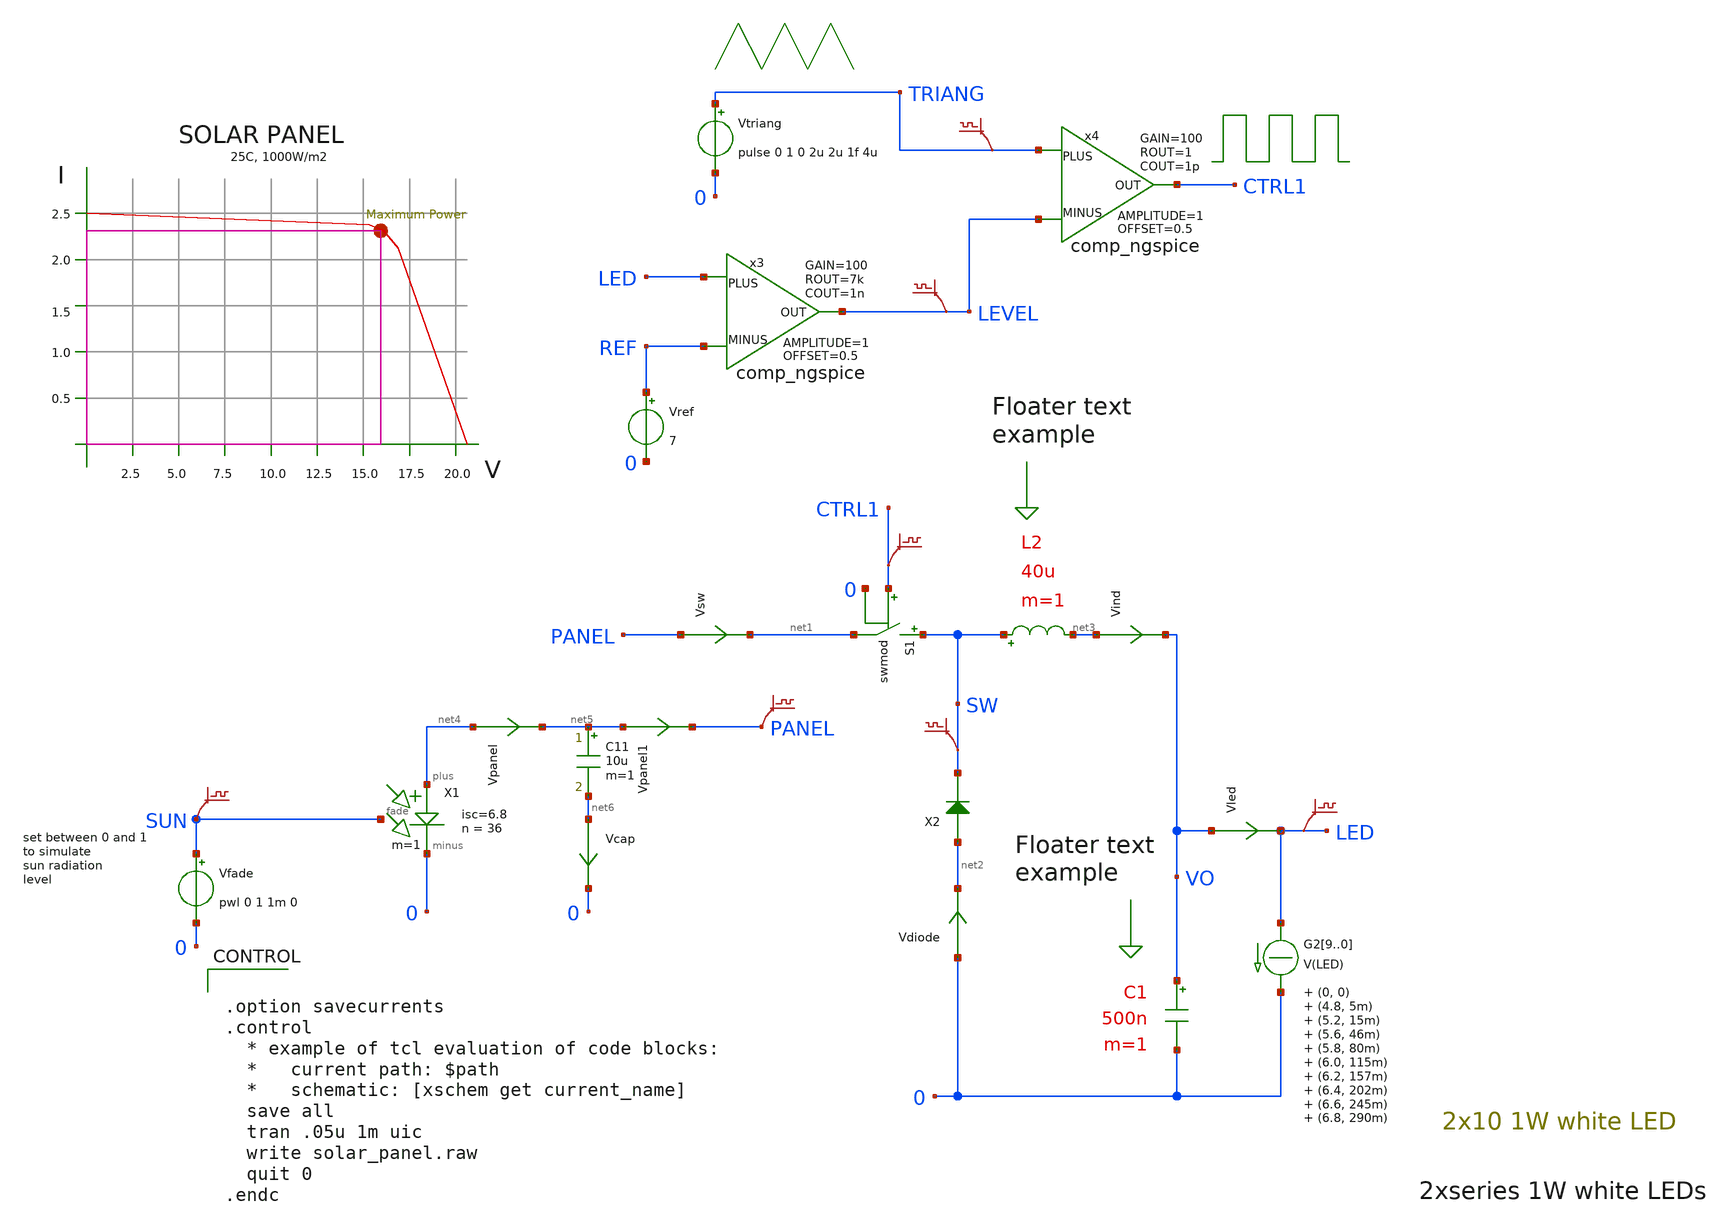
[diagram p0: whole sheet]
** sch_path: xschem_library/ngspice/solar_panel.sch
* Copyright (C) 1998-2024 Stefan Frederik Schippers
* This program is free software; you can redistribute it and/or modify
* it under the terms of the GNU General Public License as published by
* the Free Software Foundation; either version 2 of the License, or
* (at your option) any later version.
* This program is distributed in the hope that it will be useful,
* but WITHOUT ANY WARRANTY; without even the implied warranty of
* MERCHANTABILITY or FITNESS FOR A PARTICULAR PURPOSE.  See the
* GNU General Public License for more details.
* You should have received a copy of the GNU General Public License
* along with this program; if not, write to the Free Software
**.subckt solar_panel
Vled VO LED 0
.save i(vled)
L2 SW net3 40u m=1
C1 VO 0 500n m=1
Vind net3 VO 0
.save i(vind)
G29 LED 0 TABLE { V(LED) } = (0, 0) (4.8, 5m) (5.2, 15m) (5.6, 46m) (5.8, 80m) (6.0, 115m) (6.2, 157m)
+ (6.4, 202m) (6.6, 245m) (6.8, 290m) (7.0, 337m) (7.2, 395m) (7.4, 470m) (8.0, 750m)
G28 LED 0 TABLE { V(LED) } = (0, 0) (4.8, 5m) (5.2, 15m) (5.6, 46m) (5.8, 80m) (6.0, 115m) (6.2, 157m)
+ (6.4, 202m) (6.6, 245m) (6.8, 290m) (7.0, 337m) (7.2, 395m) (7.4, 470m) (8.0, 750m)
G27 LED 0 TABLE { V(LED) } = (0, 0) (4.8, 5m) (5.2, 15m) (5.6, 46m) (5.8, 80m) (6.0, 115m) (6.2, 157m)
+ (6.4, 202m) (6.6, 245m) (6.8, 290m) (7.0, 337m) (7.2, 395m) (7.4, 470m) (8.0, 750m)
G26 LED 0 TABLE { V(LED) } = (0, 0) (4.8, 5m) (5.2, 15m) (5.6, 46m) (5.8, 80m) (6.0, 115m) (6.2, 157m)
+ (6.4, 202m) (6.6, 245m) (6.8, 290m) (7.0, 337m) (7.2, 395m) (7.4, 470m) (8.0, 750m)
G25 LED 0 TABLE { V(LED) } = (0, 0) (4.8, 5m) (5.2, 15m) (5.6, 46m) (5.8, 80m) (6.0, 115m) (6.2, 157m)
+ (6.4, 202m) (6.6, 245m) (6.8, 290m) (7.0, 337m) (7.2, 395m) (7.4, 470m) (8.0, 750m)
G24 LED 0 TABLE { V(LED) } = (0, 0) (4.8, 5m) (5.2, 15m) (5.6, 46m) (5.8, 80m) (6.0, 115m) (6.2, 157m)
+ (6.4, 202m) (6.6, 245m) (6.8, 290m) (7.0, 337m) (7.2, 395m) (7.4, 470m) (8.0, 750m)
G23 LED 0 TABLE { V(LED) } = (0, 0) (4.8, 5m) (5.2, 15m) (5.6, 46m) (5.8, 80m) (6.0, 115m) (6.2, 157m)
+ (6.4, 202m) (6.6, 245m) (6.8, 290m) (7.0, 337m) (7.2, 395m) (7.4, 470m) (8.0, 750m)
G22 LED 0 TABLE { V(LED) } = (0, 0) (4.8, 5m) (5.2, 15m) (5.6, 46m) (5.8, 80m) (6.0, 115m) (6.2, 157m)
+ (6.4, 202m) (6.6, 245m) (6.8, 290m) (7.0, 337m) (7.2, 395m) (7.4, 470m) (8.0, 750m)
G21 LED 0 TABLE { V(LED) } = (0, 0) (4.8, 5m) (5.2, 15m) (5.6, 46m) (5.8, 80m) (6.0, 115m) (6.2, 157m)
+ (6.4, 202m) (6.6, 245m) (6.8, 290m) (7.0, 337m) (7.2, 395m) (7.4, 470m) (8.0, 750m)
G20 LED 0 TABLE { V(LED) } = (0, 0) (4.8, 5m) (5.2, 15m) (5.6, 46m) (5.8, 80m) (6.0, 115m) (6.2, 157m)
+ (6.4, 202m) (6.6, 245m) (6.8, 290m) (7.0, 337m) (7.2, 395m) (7.4, 470m) (8.0, 750m)
Vsw PANEL net1 0
.save i(vsw)
Vdiode 0 net2 0
.save i(vdiode)
.save v(led)
.save v(panel)
.save v(sw)
X1 net4 0 SUN pv_ngspice area=1 isc=6.8 n=36 rs=0.002 rp=40 m=1
C11 net5 net6 10u m=1
Vpanel net4 net5 0
.save i(vpanel)
X2 net2 SW diode_ngspice Ron=0.1 Roff=1e9 m=1
S1 SW net1 CTRL1 0 swmod
Vpanel1 net5 PANEL 0
.save i(vpanel1)
Vcap net6 0 0
.save i(vcap)
Vfade SUN 0 pwl 0 1 1m 0
Vtriang TRIANG 0 pulse 0 1 0 2u 2u 1f 4u
Vref REF 0 7
x3 LED LEVEL REF comp_ngspice OFFSET=0.5 AMPLITUDE=1 GAIN=100 ROUT=7k COUT=1n
x4 TRIANG CTRL1 LEVEL comp_ngspice OFFSET=0.5 AMPLITUDE=1 GAIN=100 ROUT=1 COUT=1p
.save v(triang)
.save v(level)
.save v(ctrl1)
.save v(sun)
**** begin user architecture code


.option savecurrents
.control
  * example of tcl evaluation of code blocks:
  *   current path: $path
  *   schematic: [xschem get current_name]
  save all
  tran .05u 1m uic
  write solar_panel.raw
  quit 0
.endc




.MODEL DIODE D(IS=1.139e-08 RS=0.99 CJO=9.3e-12 VJ=1.6 M=0.411 BV=30 EG=0.7 )
.MODEL swmod SW(VT=0.5 VH=0.01 RON=0.01 ROFF=10000000)


**** end user architecture code
**.ends

* expanding   symbol:  pv_ngspice.sym # of pins=3
** sym_path: xschem_library/ngspice/pv_ngspice.sym
** sch_path: xschem_library/ngspice/pv_ngspice.sch
.subckt pv_ngspice plus minus fade  isc=6 area=1 n=36 rs=0.002 rp=40
*.iopin minus
*.ipin fade
*.iopin plus
Vf net1 A 0
.save i(vf)
Vm minus im 0
.save i(vm)
Vp ip plus 0
.save i(vp)
D1 A 0 DPANEL area='area'
Rp net2 0 'rp' m=1
Rs B net3 'rs' m=1
F1 0 B e1 1
E1 ip im B 0 'n'
Vf1 fade F 0
.save i(vf1)
B1 0 net1 I = v(f) * isc
Vr A net2 0
.save i(vr)
Vm1 net2 net3 0
.save i(vm1)
.ends


* expanding   symbol:  diode_ngspice.sym # of pins=2
** sym_path: xschem_library/ngspice/diode_ngspice.sym
** sch_path: xschem_library/ngspice/diode_ngspice.sch
.subckt diode_ngspice plus minus   Roff=1e9 Ron=0.1
*.iopin plus
*.iopin minus
Vm mn minus 0
.save i(vm)
Vp plus pn 0
.save i(vp)
B1 pn mn I = 'v(pn,mn) > 0 ? v(pn,mn) / Ron : v(pn,mn) / Roff'
.ends


* expanding   symbol:  comp_ngspice.sym # of pins=3
** sym_path: xschem_library/ngspice/comp_ngspice.sym
** sch_path: xschem_library/ngspice/comp_ngspice.sch
.subckt comp_ngspice PLUS OUT MINUS  OFFSET=0 AMPLITUDE=5 GAIN=100 ROUT=1000 COUT=1p
*.ipin PLUS
*.ipin MINUS
*.opin OUT
B1 IOUT 0 V = {OFFSET + AMPLITUDE/2*(tanh(V(IPLUS,IMINUS)*GAIN*2/AMPLITUDE))}
R1 OUT IOUT {ROUT} m=1
C3 OUT 0 {COUT} m=1
V1 IPLUS PLUS 0
V2 IMINUS MINUS 0
.ends

**** begin user architecture code
.model DPANEL D IS=1n N=1
**** end user architecture code
.end
